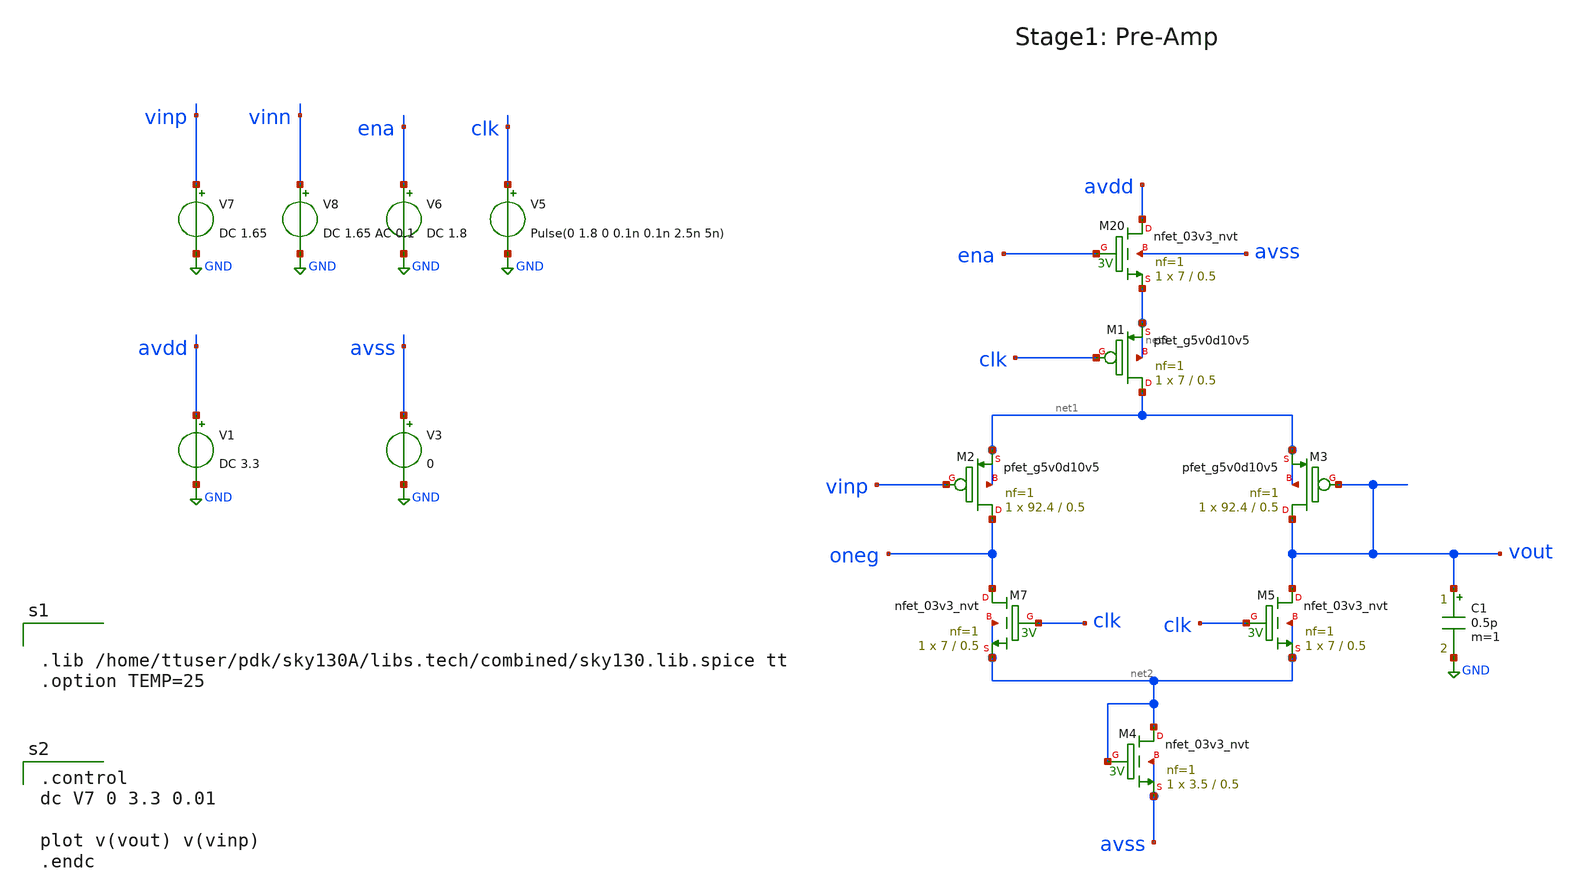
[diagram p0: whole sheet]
** sch_path: xschem/icmr_tb.sch
**.subckt icmr_tb
XM1 net1 clk net3 net3 sky130_fd_pr__pfet_g5v0d10v5 L=0.5 W=7 nf=1 ad='int((nf+1)/2) * W/nf * 0.29' as='int((nf+2)/2) * W/nf * 0.29'
+ pd='2*int((nf+1)/2) * (W/nf + 0.29)' ps='2*int((nf+2)/2) * (W/nf + 0.29)' nrd='0.29 / W' nrs='0.29 / W'
+ sa=0 sb=0 sd=0 mult=1 m=1
XM2 oneg vinp net1 net1 sky130_fd_pr__pfet_g5v0d10v5 L=0.5 W=92.4 nf=1 ad='int((nf+1)/2) * W/nf * 0.29'
+ as='int((nf+2)/2) * W/nf * 0.29' pd='2*int((nf+1)/2) * (W/nf + 0.29)' ps='2*int((nf+2)/2) * (W/nf + 0.29)'
+ nrd='0.29 / W' nrs='0.29 / W' sa=0 sb=0 sd=0 mult=1 m=1
XM3 vout vout net1 net1 sky130_fd_pr__pfet_g5v0d10v5 L=0.5 W=92.4 nf=1 ad='int((nf+1)/2) * W/nf * 0.29'
+ as='int((nf+2)/2) * W/nf * 0.29' pd='2*int((nf+1)/2) * (W/nf + 0.29)' ps='2*int((nf+2)/2) * (W/nf + 0.29)'
+ nrd='0.29 / W' nrs='0.29 / W' sa=0 sb=0 sd=0 mult=1 m=1
XM7 oneg clk net2 net2 sky130_fd_pr__nfet_03v3_nvt L=0.5 W=7 nf=1 ad='int((nf+1)/2) * W/nf * 0.29' as='int((nf+2)/2) * W/nf * 0.29'
+ pd='2*int((nf+1)/2) * (W/nf + 0.29)' ps='2*int((nf+2)/2) * (W/nf + 0.29)' nrd='0.29 / W' nrs='0.29 / W'
+ sa=0 sb=0 sd=0 mult=1 m=1
XM5 vout clk net2 net2 sky130_fd_pr__nfet_03v3_nvt L=0.5 W=7 nf=1 ad='int((nf+1)/2) * W/nf * 0.29' as='int((nf+2)/2) * W/nf * 0.29'
+ pd='2*int((nf+1)/2) * (W/nf + 0.29)' ps='2*int((nf+2)/2) * (W/nf + 0.29)' nrd='0.29 / W' nrs='0.29 / W'
+ sa=0 sb=0 sd=0 mult=1 m=1
XM4 net2 net2 avss avss sky130_fd_pr__nfet_03v3_nvt L=0.5 W=3.5 nf=1 ad='int((nf+1)/2) * W/nf * 0.29'
+ as='int((nf+2)/2) * W/nf * 0.29' pd='2*int((nf+1)/2) * (W/nf + 0.29)' ps='2*int((nf+2)/2) * (W/nf + 0.29)'
+ nrd='0.29 / W' nrs='0.29 / W' sa=0 sb=0 sd=0 mult=1 m=1
XM20 avdd ena net3 avss sky130_fd_pr__nfet_03v3_nvt L=0.5 W=7 nf=1 ad='int((nf+1)/2) * W/nf * 0.29' as='int((nf+2)/2) * W/nf * 0.29'
+ pd='2*int((nf+1)/2) * (W/nf + 0.29)' ps='2*int((nf+2)/2) * (W/nf + 0.29)' nrd='0.29 / W' nrs='0.29 / W'
+ sa=0 sb=0 sd=0 mult=1 m=1
V1 avdd GND DC 3.3
V3 avss GND 0
V5 clk GND Pulse(0 1.8 0 0.1n 0.1n 2.5n 5n)
V6 ena GND DC 1.8
V7 vinp GND DC 1.65
V8 vinn GND DC 1.65 AC 0.1
C1 vout GND 0.5p m=1
**** begin user architecture code


.lib /home/ttuser/pdk/sky130A/libs.tech/combined/sky130.lib.spice tt
.option TEMP=25


.control
dc V7 0 3.3 0.01

plot v(vout) v(vinp)
.endc

**** end user architecture code
**.ends
.GLOBAL GND
.end
